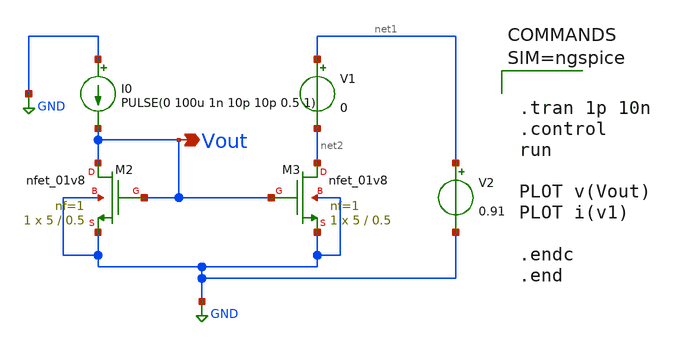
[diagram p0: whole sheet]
** sch_path: sch/Current_mirror_NMOS.sch
**.subckt Current_mirror_NMOS Vout
*.opin Vout
XM3 net2 Vout GND GND sky130_fd_pr__nfet_01v8 L=0.5 W=5 nf=1 ad='int((1 + 1)/2) * 5 / 1 * 0.29' as='int((1 + 2)/2) * 5 / 1 * 0.29'
+ pd='2*int((1 + 1)/2) * (5 / 1 + 0.29)' ps='2*int((1 + 2)/2) * (5 / 1 + 0.29)' nrd='0.29 / 5 ' nrs='0.29 / 5 '
+ sa=0 sb=0 sd=0 mult=1 m=1
XM2 Vout Vout GND GND sky130_fd_pr__nfet_01v8 L=0.5 W=5 nf=1 ad='int((1 + 1)/2) * 5 / 1 * 0.29' as='int((1 + 2)/2) * 5 / 1 * 0.29'
+ pd='2*int((1 + 1)/2) * (5 / 1 + 0.29)' ps='2*int((1 + 2)/2) * (5 / 1 + 0.29)' nrd='0.29 / 5 ' nrs='0.29 / 5 '
+ sa=0 sb=0 sd=0 mult=1 m=1
I0 GND Vout PULSE(0 100u 1n 10p 10p 0.5 1)
V1 net1 net2 0
V2 net1 GND 0.91
**** begin user architecture code

** opencircuitdesign pdks install
.lib $::SKYWATER_MODELS/sky130.lib.spice tt




.tran 1p 10n
.control
run

PLOT v(Vout)
PLOT i(v1)

.endc
.end



**** end user architecture code
**.ends
.GLOBAL GND
.end
